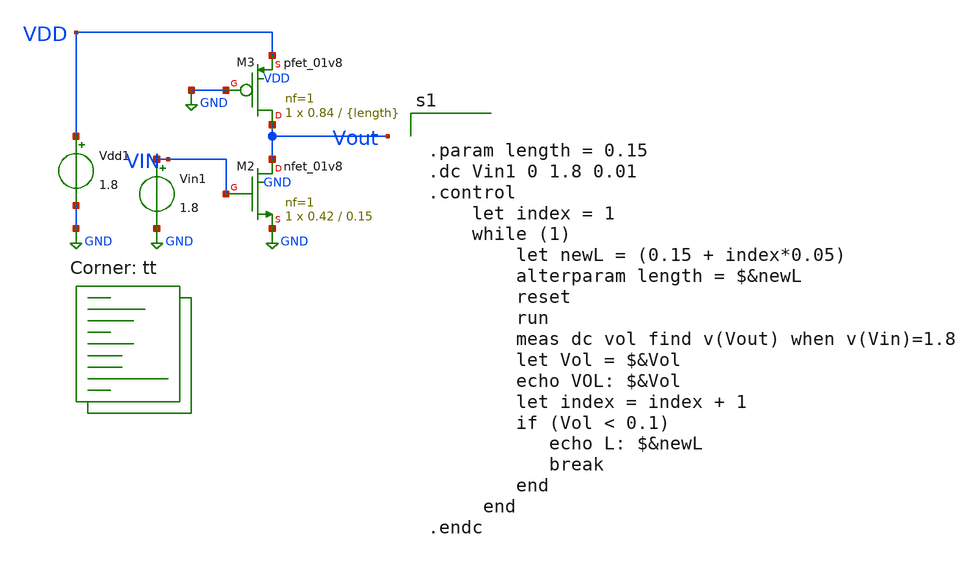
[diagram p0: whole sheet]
** sch_path: tutorial_3/tutorial_3_2m1.sch
**.subckt tutorial_3_2m1
XM2 Vout VIN GND GND sky130_fd_pr__nfet_01v8 L=0.15 W=0.42 nf=1 ad='int((nf+1)/2) * W/nf * 0.29' as='int((nf+2)/2) * W/nf * 0.29'
+ pd='2*int((nf+1)/2) * (W/nf + 0.29)' ps='2*int((nf+2)/2) * (W/nf + 0.29)' nrd='0.29 / W' nrs='0.29 / W'
+ sa=0 sb=0 sd=0 mult=1 m=1
XM3 Vout GND VDD VDD sky130_fd_pr__pfet_01v8 L={length} W=0.84 nf=1 ad='int((nf+1)/2) * W/nf * 0.29'
+ as='int((nf+2)/2) * W/nf * 0.29' pd='2*int((nf+1)/2) * (W/nf + 0.29)' ps='2*int((nf+2)/2) * (W/nf + 0.29)'
+ nrd='0.29 / W' nrs='0.29 / W' sa=0 sb=0 sd=0 mult=1 m=1
Vin1 VIN GND 1.8
Vdd1 VDD GND 1.8
**** begin user architecture code
.lib $::SKYWATER_MODELS/sky130.lib.spice tt


.param length = 0.15
.dc Vin1 0 1.8 0.01
.control
    let index = 1
    while (1)
        let newL = (0.15 + index*0.05)
        alterparam length = $&newL
        reset
        run
        meas dc vol find v(Vout) when v(Vin)=1.8
        let Vol = $&Vol
        echo VOL: $&Vol
        let index = index + 1
        if (Vol < 0.1)
           echo L: $&newL
           break
        end
     end
.endc

**** end user architecture code
**.ends
.GLOBAL GND
.end
